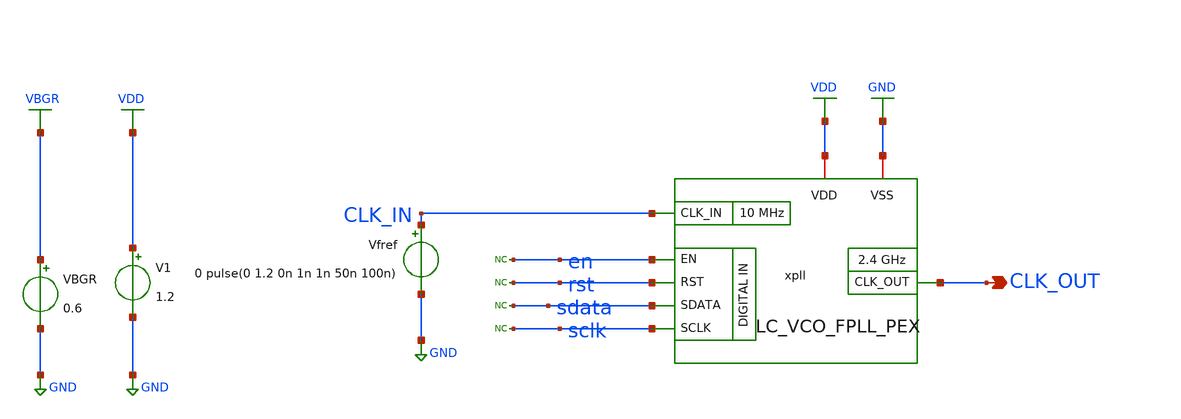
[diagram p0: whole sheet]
** sch_path: xschem/top-pll/LC_VCO_FPLL_PEX_tb.sch
**.subckt LC_VCO_FPLL_PEX_tb CLK_OUT
*.opin CLK_OUT
V1 VDD GND 1.2
Vfref CLK_IN GND 0 pulse(0 1.2 0n 1n 1n 50n 100n)
VBGR VBGR GND 0.6
xpll CLK_IN VDD CLK_OUT GND en rst sdata sclk LC_VCO_FPLL_PEX
* noconn en
* noconn rst
* noconn sdata
* noconn sclk
**** begin user architecture code



*****************************************************
* PLL + DSM Frequency Divider Testbench (Optimized)
*****************************************************

.option temp=27
.param VDD=1.2
.option rshunt = 1.0e12

* ==============================
* Include Models & Stimuli
* ==============================
.include 4nH_INDUCTOR.spice
.include ../simulations/stimuli_test.cir
* start-up kick: a noise-free run can stay at the unstable equilibrium at low VCTRL
.ic v(xpll.outp)=0.4
* extracted (Magic RC) netlists of every block; the inductor is the EM model
.include ../pex/PHASE_FREQ_DET__PHASE_FREQ_DET/magic_RC/PHASE_FREQ_DET.pex.spice
.include ../pex/CHARGE_PUMP_V2__CHARGE_PUMP/magic_RC/CHARGE_PUMP.pex.spice
.include ../pex/LOOP_FILTER__LOOP_FILTER/magic_RC/LOOP_FILTER.pex.spice
.include ../pex/LC_VCO_NOIND__LC_VCO_NOIND/magic_RC/LC_VCO_NOIND.pex_sim.spice
* layout-extracted netlist straight from the OpenLane run. The PDK standard cells are included
*+ first, so the
* black-box entries at the top of the OpenLane file are ignored (ngspice keeps the first
*+ definition).
.include /foss/pdks/ihp-sg13g2/libs.ref/sg13g2_stdcell/spice/sg13g2_stdcell.spice
.include /foss/designs/unicasss-tools/SG13G2_2.4GHz_LC_VCO_FPLL/xschem/dsm/src/runs/RUN_2026-03-04_15-08-00/final/spice/dsm_and_freq_divider.spice
.subckt DSM_N_FREQ_DIV_PEX freq_in rst sclk sdata en freq_out VDD GND
x0 GND VDD en freq_in freq_out rst sclk sdata dsm_and_freq_divider
.ends
.include ../pex/BANDGAP_REF__BANDGAP_REF/magic_RC/BANDGAP_REF.pex.spice

* ==============================
* Simulation Options (Optimized for Speed & Stability)
* ==============================
* gear method improves stability for long oscillator runs
* reltol=1e-3 prevents the simulator from bogging down on microscopic errors
.options reltol=1e-3 abstol=1e-9 vntol=1e-6 method=gear

.control
  * CRITICAL: Save ONLY essential low-frequency signals.
  save xpll.vctrl xpll.up xpll.dn xpll.clk_fb clk_out clk_in vbgr xpll.vcp xpll.outp sdata sclk en
+ rst


  * 20p defines the step to resolve the 2.4 GHz edges without forcing a maxstep.
  tran 10p 40u

  remzerovec
  write tb_LC_VCO_FPLL_PEX_40u.raw
.endc






.lib cornerMOSlv.lib mos_tt
.lib cornerMOShv.lib mos_tt
.lib cornerHBT.lib hbt_typ
.lib cornerRES.lib res_typ
.lib cornerCAP.lib cap_typ
.include /foss/pdks/ihp-sg13g2/libs.ref/sg13g2_stdcell/spice/sg13g2_stdcell.spice
*.include /opt/pdks/ihp-sg13g2/libs.ref/sg13g2_stdcell/spice/sg13g2_stdcell.spice
.global VDD GND




**** end user architecture code
**.ends
.GLOBAL GND
.GLOBAL VDD
.GLOBAL VBGR
.end
